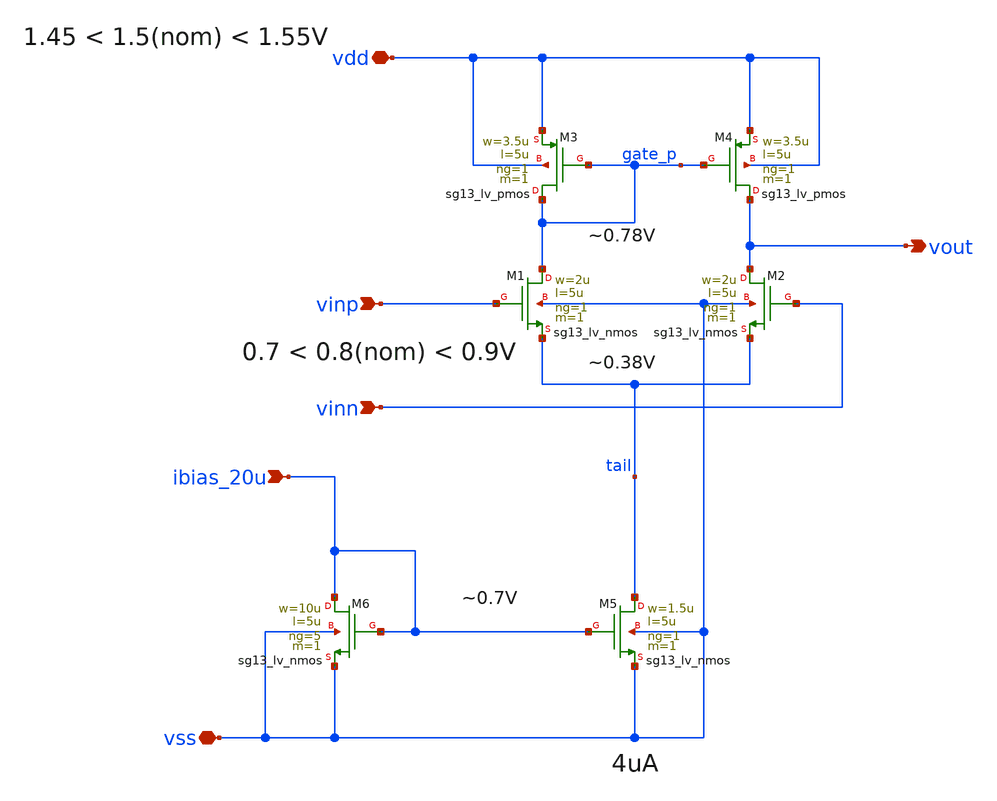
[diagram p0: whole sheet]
** sch_path: 004_Real_Circuits/002_version_no_enable/ota-5t_no_ena_copy.sch
**.subckt ota-5t_no_ena_copy vout vdd vinp vinn ibias_20u vss
*.opin vout
*.iopin vdd
*.ipin vinp
*.ipin vinn
*.ipin ibias_20u
*.iopin vss
XM5 tail ibias_20u vss vss sg13_lv_nmos w=1.5u l=5u ng=1 m=1 mm_ok=1
XM4 vout gate_p vdd vdd sg13_lv_pmos w=3.5u l=5u ng=1 m=1 mm_ok=1
XM1 gate_p vinp tail vss sg13_lv_nmos w=2u l=5u ng=1 m=1 mm_ok=1
XM2 vout vinn tail vss sg13_lv_nmos w=2u l=5u ng=1 m=1 mm_ok=1
XM3 gate_p gate_p vdd vdd sg13_lv_pmos w=3.5u l=5u ng=1 m=1 mm_ok=1
XM6 ibias_20u ibias_20u vss vss sg13_lv_nmos w=10u l=5u ng=5 m=1 mm_ok=1
**.ends
.end
